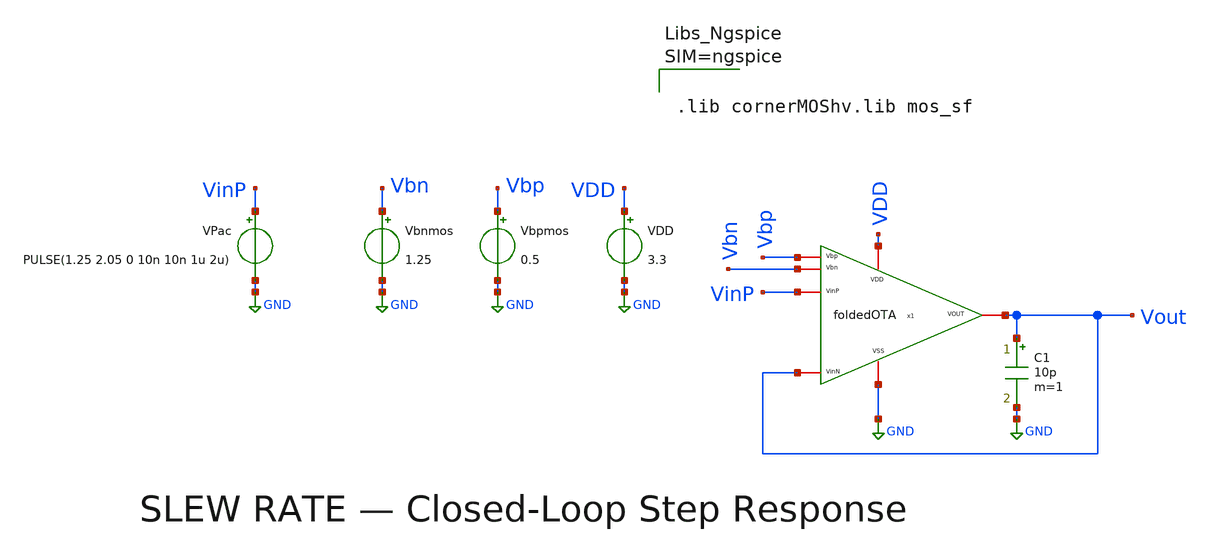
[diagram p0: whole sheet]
** sch_path: v1_ideal_current_sources/slew_rate/SR-foldedOTA.sch
* v1_ideal_current_sources/schematic/foldedOTA.sch:
* (c) 2026 Fares Satouh
**.subckt SR-foldedOTA
VPac VinP GND PULSE(1.25 2.05 0 10n 10n 1u 2u)
Vbnmos Vbn GND 1.25
Vbpmos Vbp GND 0.5
VDD VDD GND 3.3
x1 VDD Vbp Vout VinP Vout Vbn GND foldedOTA
C1 Vout GND 10p m=1
**** begin user architecture code



.lib cornerMOShv.lib mos_sf





.control
destroy all
tran 1n 2u
run
save all

meas tran sr_rise_td trig v(vout) val=1.33 rise=1 targ v(vout) val=1.97 rise=1
meas tran sr_fall_td trig v(vout) val=1.97 fall=1 targ v(vout) val=1.33 fall=1

let sr_rise = 0.64 / sr_rise_td
let sr_fall = 0.64 / sr_fall_td

plot v(vinp) v(vout) ylabel 'Voltage (V)' title 'Slew Rate Step Response'
echo
echo '================ SLEW RATE SUMMARY ================'
print sr_rise
print sr_fall
echo '====================================================='
.endc


**** end user architecture code
**.ends

* expanding   symbol:  foldedOTA.sym # of pins=7
** sym_path: v1_ideal_current_sources/schematic/foldedOTA.sym
** sch_path: v1_ideal_current_sources/schematic/foldedOTA.sch
.subckt foldedOTA VDD Vbp VOUT VinP VinN Vbn VSS
*.iopin VDD
*.iopin VSS
*.iopin VOUT
*.iopin Vbp
*.iopin Vbn
*.iopin VinN
*.iopin VinP
XM1 net2 VinP net1 VSS sg13_hv_nmos w=28u l=1u ng=4 m=1 mm_ok=1
XM2 net3 VinN net1 VSS sg13_hv_nmos w=28u l=1u ng=4 m=1 mm_ok=1
XM3 net1 net8 VSS VSS sg13_hv_nmos w=15u l=1u ng=3 m=1 mm_ok=1
XM4 net2 net7 VDD VDD sg13_hv_pmos w=14u l=1u ng=2 m=1 mm_ok=1
XM5 net3 net7 VDD VDD sg13_hv_pmos w=14u l=1u ng=2 m=1 mm_ok=1
XM6 net4 Vbp net2 VDD sg13_hv_pmos w=2u l=1u ng=1 m=1 mm_ok=1
XM7 VOUT Vbp net3 VDD sg13_hv_pmos w=2u l=1u ng=1 m=1 mm_ok=1
XM8 net4 Vbn net5 VSS sg13_hv_nmos w=7u l=1u ng=1 m=1 mm_ok=1
XM9 VOUT Vbn net6 VSS sg13_hv_nmos w=7u l=1u ng=1 m=1 mm_ok=1
XM10 net5 net4 VSS VSS sg13_hv_nmos w=7u l=1u ng=1 m=1 mm_ok=1
XM11 net6 net4 VSS VSS sg13_hv_nmos w=7u l=1u ng=1 m=1 mm_ok=1
XM12 net8 net8 VSS VSS sg13_hv_nmos w=15u l=1u ng=3 m=1 mm_ok=1
I0 VDD net8 50u
XM13 net7 net7 VDD VDD sg13_hv_pmos w=14u l=1u ng=2 m=1 mm_ok=1
I1 net7 VSS 50u
.ends

.GLOBAL GND
.end
